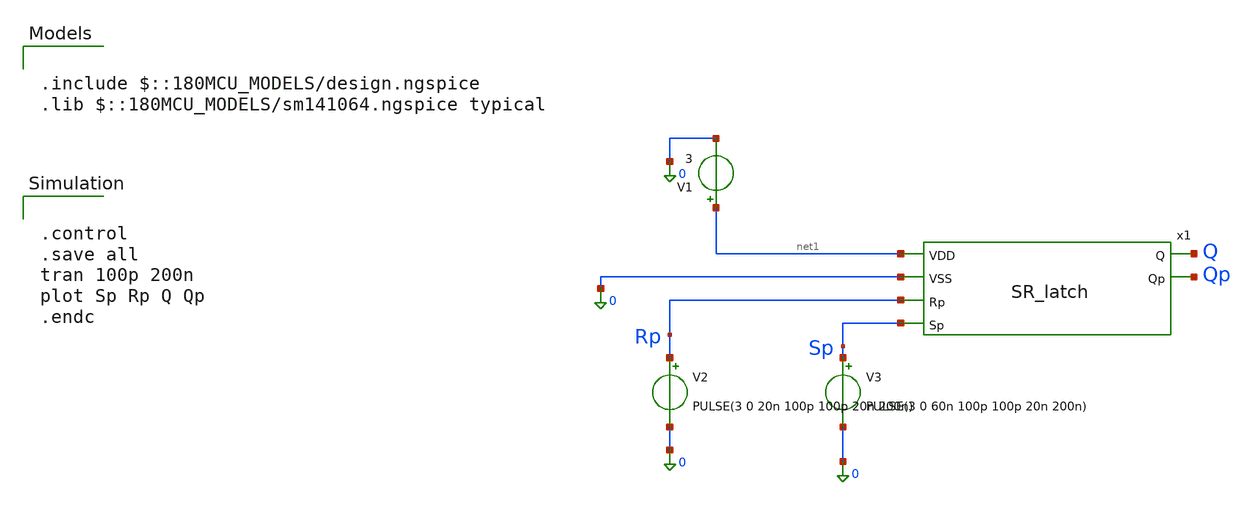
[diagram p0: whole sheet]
** sch_path: designs/libs/tb_analog/tb_SR_Latch/tb_SR_latch.sch
**.subckt tb_SR_latch
x1 Q net1 0 Qp Rp Sp SR_latch
V1 net1 0 3
V2 Rp 0 PULSE(3 0 20n 100p 100p 20n 200n)
V3 Sp 0 PULSE(3 0 60n 100p 100p 20n 200n)
**** begin user architecture code

.include $::180MCU_MODELS/design.ngspice
.lib $::180MCU_MODELS/sm141064.ngspice typical



.control
.save all
tran 100p 200n
plot Sp Rp Q Qp
.endc


**** end user architecture code
**.ends
.end
